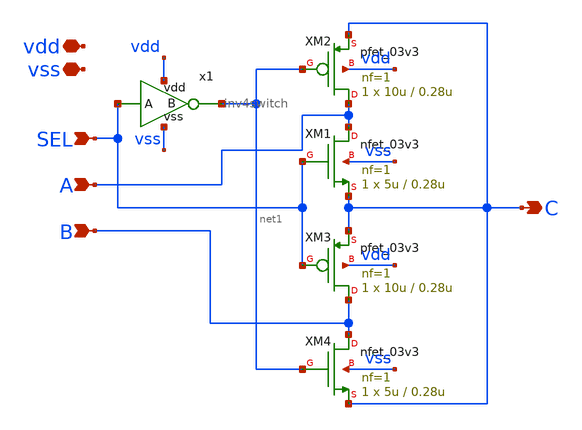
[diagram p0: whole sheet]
** sch_path: General/ADC/switching/mux_2to1.sch
**.subckt mux_2to1 A B SEL C vdd vss
*.ipin A
*.ipin B
*.ipin SEL
*.opin C
*.iopin vdd
*.iopin vss
XM1 A SEL C vss nfet_03v3 L=0.28u W=5u nf=1 ad='int((nf+1)/2) * W/nf * 0.18u' as='int((nf+2)/2) * W/nf * 0.18u'
+ pd='2*int((nf+1)/2) * (W/nf + 0.18u)' ps='2*int((nf+2)/2) * (W/nf + 0.18u)' nrd='0.18u / W' nrs='0.18u / W'
+ sa=0 sb=0 sd=0 m=1
XM2 A net1 C vdd pfet_03v3 L=0.28u W=10u nf=1 ad='int((nf+1)/2) * W/nf * 0.18u' as='int((nf+2)/2) * W/nf * 0.18u'
+ pd='2*int((nf+1)/2) * (W/nf + 0.18u)' ps='2*int((nf+2)/2) * (W/nf + 0.18u)' nrd='0.18u / W' nrs='0.18u / W'
+ sa=0 sb=0 sd=0 m=1
XM3 B SEL C vdd pfet_03v3 L=0.28u W=10u nf=1 ad='int((nf+1)/2) * W/nf * 0.18u' as='int((nf+2)/2) * W/nf * 0.18u'
+ pd='2*int((nf+1)/2) * (W/nf + 0.18u)' ps='2*int((nf+2)/2) * (W/nf + 0.18u)' nrd='0.18u / W' nrs='0.18u / W'
+ sa=0 sb=0 sd=0 m=1
XM4 B net1 C vss nfet_03v3 L=0.28u W=5u nf=1 ad='int((nf+1)/2) * W/nf * 0.18u' as='int((nf+2)/2) * W/nf * 0.18u'
+ pd='2*int((nf+1)/2) * (W/nf + 0.18u)' ps='2*int((nf+2)/2) * (W/nf + 0.18u)' nrd='0.18u / W' nrs='0.18u / W'
+ sa=0 sb=0 sd=0 m=1
x1 net1 SEL vdd vss inv4switch
**.ends

* expanding   symbol:  adc/switching/inv4switch.sym # of pins=4
** sym_path: General/ADC/switching/inv4switch.sym
** sch_path: General/ADC/switching/inv4switch.sch
.subckt inv4switch B A vdd vss
*.ipin A
*.opin B
*.iopin vdd
*.iopin vss
XM1 B A vss vss nfet_03v3 L=0.3u W=1u nf=1 ad='int((nf+1)/2) * W/nf * 0.18u' as='int((nf+2)/2) * W/nf * 0.18u'
+ pd='2*int((nf+1)/2) * (W/nf + 0.18u)' ps='2*int((nf+2)/2) * (W/nf + 0.18u)' nrd='0.18u / W' nrs='0.18u / W'
+ sa=0 sb=0 sd=0 m=1
XM2 B A vdd vdd pfet_03v3 L=0.3u W=2u nf=1 ad='int((nf+1)/2) * W/nf * 0.18u' as='int((nf+2)/2) * W/nf * 0.18u'
+ pd='2*int((nf+1)/2) * (W/nf + 0.18u)' ps='2*int((nf+2)/2) * (W/nf + 0.18u)' nrd='0.18u / W' nrs='0.18u / W'
+ sa=0 sb=0 sd=0 m=1
.ends

.end
